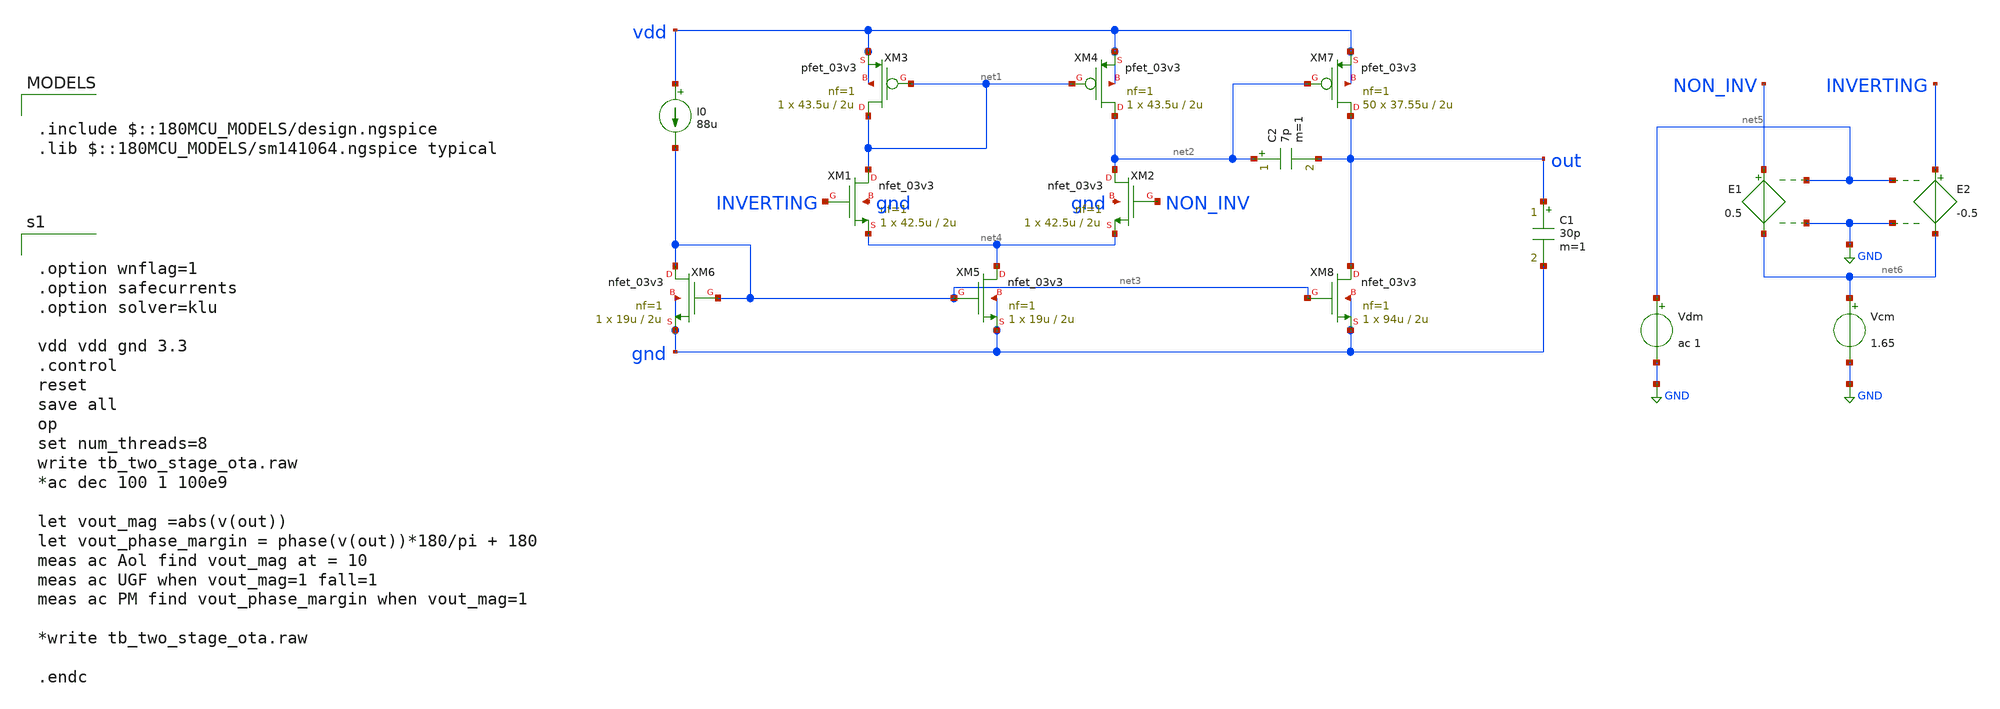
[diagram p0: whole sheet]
** sch_path: designs/libs/tb_analog/tb_ts_miller_ota/two_stage_ota.sch
**.subckt two_stage_ota
XM1 net1 INVERTING net4 gnd nfet_03v3 L=2u W=42.5u nf=1 ad='int((nf+1)/2) * W/nf * 0.18u' as='int((nf+2)/2) * W/nf * 0.18u'
+ pd='2*int((nf+1)/2) * (W/nf + 0.18u)' ps='2*int((nf+2)/2) * (W/nf + 0.18u)' nrd='0.18u / W' nrs='0.18u / W'
+ sa=0 sb=0 sd=0 m=1
XM3 net1 net1 vdd vdd pfet_03v3 L=2u W=43.5u nf=1 ad='int((nf+1)/2) * W/nf * 0.18u' as='int((nf+2)/2) * W/nf * 0.18u'
+ pd='2*int((nf+1)/2) * (W/nf + 0.18u)' ps='2*int((nf+2)/2) * (W/nf + 0.18u)' nrd='0.18u / W' nrs='0.18u / W'
+ sa=0 sb=0 sd=0 m=1
XM5 net4 net3 gnd gnd nfet_03v3 L=2u W=19u nf=1 ad='int((nf+1)/2) * W/nf * 0.18u' as='int((nf+2)/2) * W/nf * 0.18u'
+ pd='2*int((nf+1)/2) * (W/nf + 0.18u)' ps='2*int((nf+2)/2) * (W/nf + 0.18u)' nrd='0.18u / W' nrs='0.18u / W'
+ sa=0 sb=0 sd=0 m=1
XM6 net3 net3 gnd gnd nfet_03v3 L=2u W=19u nf=1 ad='int((nf+1)/2) * W/nf * 0.18u' as='int((nf+2)/2) * W/nf * 0.18u'
+ pd='2*int((nf+1)/2) * (W/nf + 0.18u)' ps='2*int((nf+2)/2) * (W/nf + 0.18u)' nrd='0.18u / W' nrs='0.18u / W'
+ sa=0 sb=0 sd=0 m=1
I0 vdd net3 88u
XM7 out net2 vdd vdd pfet_03v3 L=2u W=37.55u nf=1 ad='int((nf+1)/2) * W/nf * 0.18u' as='int((nf+2)/2) * W/nf * 0.18u'
+ pd='2*int((nf+1)/2) * (W/nf + 0.18u)' ps='2*int((nf+2)/2) * (W/nf + 0.18u)' nrd='0.18u / W' nrs='0.18u / W'
+ sa=0 sb=0 sd=0 m=50
XM8 out net3 gnd gnd nfet_03v3 L=2u W=94u nf=1 ad='int((nf+1)/2) * W/nf * 0.18u' as='int((nf+2)/2) * W/nf * 0.18u'
+ pd='2*int((nf+1)/2) * (W/nf + 0.18u)' ps='2*int((nf+2)/2) * (W/nf + 0.18u)' nrd='0.18u / W' nrs='0.18u / W'
+ sa=0 sb=0 sd=0 m=1
C1 out gnd 30p m=1
C2 net2 out 7p m=1
XM2 net2 NON_INV net4 gnd nfet_03v3 L=2u W=42.5u nf=1 ad='int((nf+1)/2) * W/nf * 0.18u' as='int((nf+2)/2) * W/nf * 0.18u'
+ pd='2*int((nf+1)/2) * (W/nf + 0.18u)' ps='2*int((nf+2)/2) * (W/nf + 0.18u)' nrd='0.18u / W' nrs='0.18u / W'
+ sa=0 sb=0 sd=0 m=1
XM4 net2 net1 vdd vdd pfet_03v3 L=2u W=43.5u nf=1 ad='int((nf+1)/2) * W/nf * 0.18u' as='int((nf+2)/2) * W/nf * 0.18u'
+ pd='2*int((nf+1)/2) * (W/nf + 0.18u)' ps='2*int((nf+2)/2) * (W/nf + 0.18u)' nrd='0.18u / W' nrs='0.18u / W'
+ sa=0 sb=0 sd=0 m=1
E1 NON_INV net6 net5 GND 0.5
E2 INVERTING net6 net5 GND -0.5
Vdm net5 GND ac 1
Vcm net6 GND 1.65
**** begin user architecture code


.option wnflag=1
.option safecurrents
.option solver=klu

vdd vdd gnd 3.3
.control
reset
save all
op
set num_threads=8
write tb_two_stage_ota.raw
*ac dec 100 1 100e9

let vout_mag =abs(v(out))
let vout_phase_margin = phase(v(out))*180/pi + 180
meas ac Aol find vout_mag at = 10
meas ac UGF when vout_mag=1 fall=1
meas ac PM find vout_phase_margin when vout_mag=1

*write tb_two_stage_ota.raw

.endc



.include $::180MCU_MODELS/design.ngspice
.lib $::180MCU_MODELS/sm141064.ngspice typical

**** end user architecture code
**.ends
.GLOBAL GND
.end
